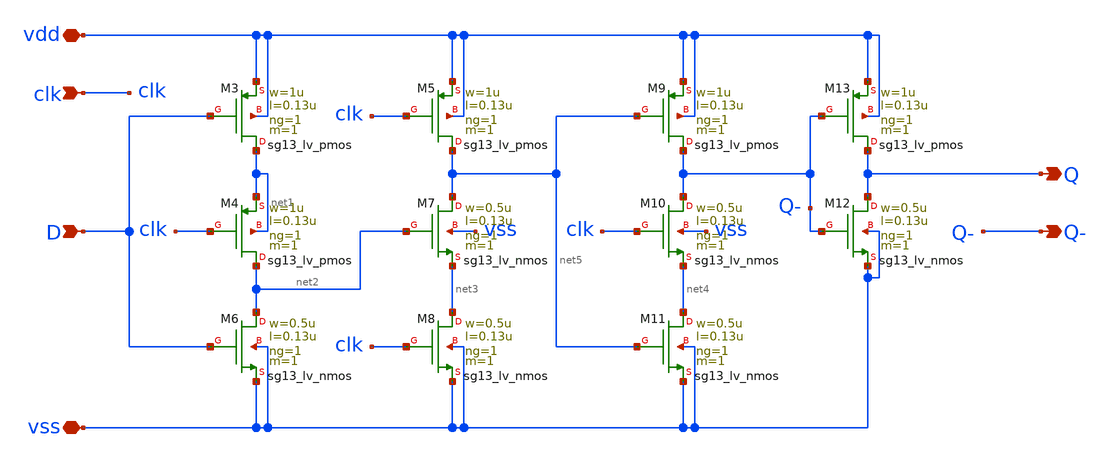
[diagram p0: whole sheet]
** sch_path: SSDOR_1.2V_v2/components/cgenerator/dff2.sch
**.subckt dff2 D vdd vss clk Q- Q
*.ipin D
*.iopin vdd
*.iopin vss
*.ipin clk
*.opin Q-
*.opin Q
XM3 net1 D vdd vdd sg13_lv_pmos w=1u l=0.13u ng=1 m=1 mm_ok=1
XM4 net2 clk net1 net1 sg13_lv_pmos w=1u l=0.13u ng=1 m=1 mm_ok=1
XM5 net5 clk vdd vdd sg13_lv_pmos w=1u l=0.13u ng=1 m=1 mm_ok=1
XM6 net2 D vss vss sg13_lv_nmos w=0.5u l=0.13u ng=1 m=1 mm_ok=1
XM7 net5 net2 net3 vss sg13_lv_nmos w=0.5u l=0.13u ng=1 m=1 mm_ok=1
XM8 net3 clk vss vss sg13_lv_nmos w=0.5u l=0.13u ng=1 m=1 mm_ok=1
XM9 Q- net5 vdd vdd sg13_lv_pmos w=1u l=0.13u ng=1 m=1 mm_ok=1
XM10 Q- clk net4 vss sg13_lv_nmos w=0.5u l=0.13u ng=1 m=1 mm_ok=1
XM11 net4 net5 vss vss sg13_lv_nmos w=0.5u l=0.13u ng=1 m=1 mm_ok=1
XM12 Q Q- vss vss sg13_lv_nmos w=0.5u l=0.13u ng=1 m=1 mm_ok=1
XM13 Q Q- vdd vdd sg13_lv_pmos w=1u l=0.13u ng=1 m=1 mm_ok=1
**.ends
.end
